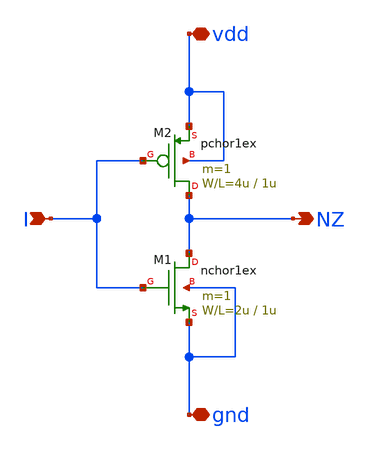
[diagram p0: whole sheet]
** sch_path: member_project/ckdur/inv.sch
**.subckt inv I NZ vdd gnd
*.ipin I
*.opin NZ
*.iopin vdd
*.iopin gnd
M1 NZ I gnd gnd nchor1ex L=1u W=2u m=1
M2 NZ I vdd vdd pchor1ex L=1u W=4u m=1
**.ends
.end
